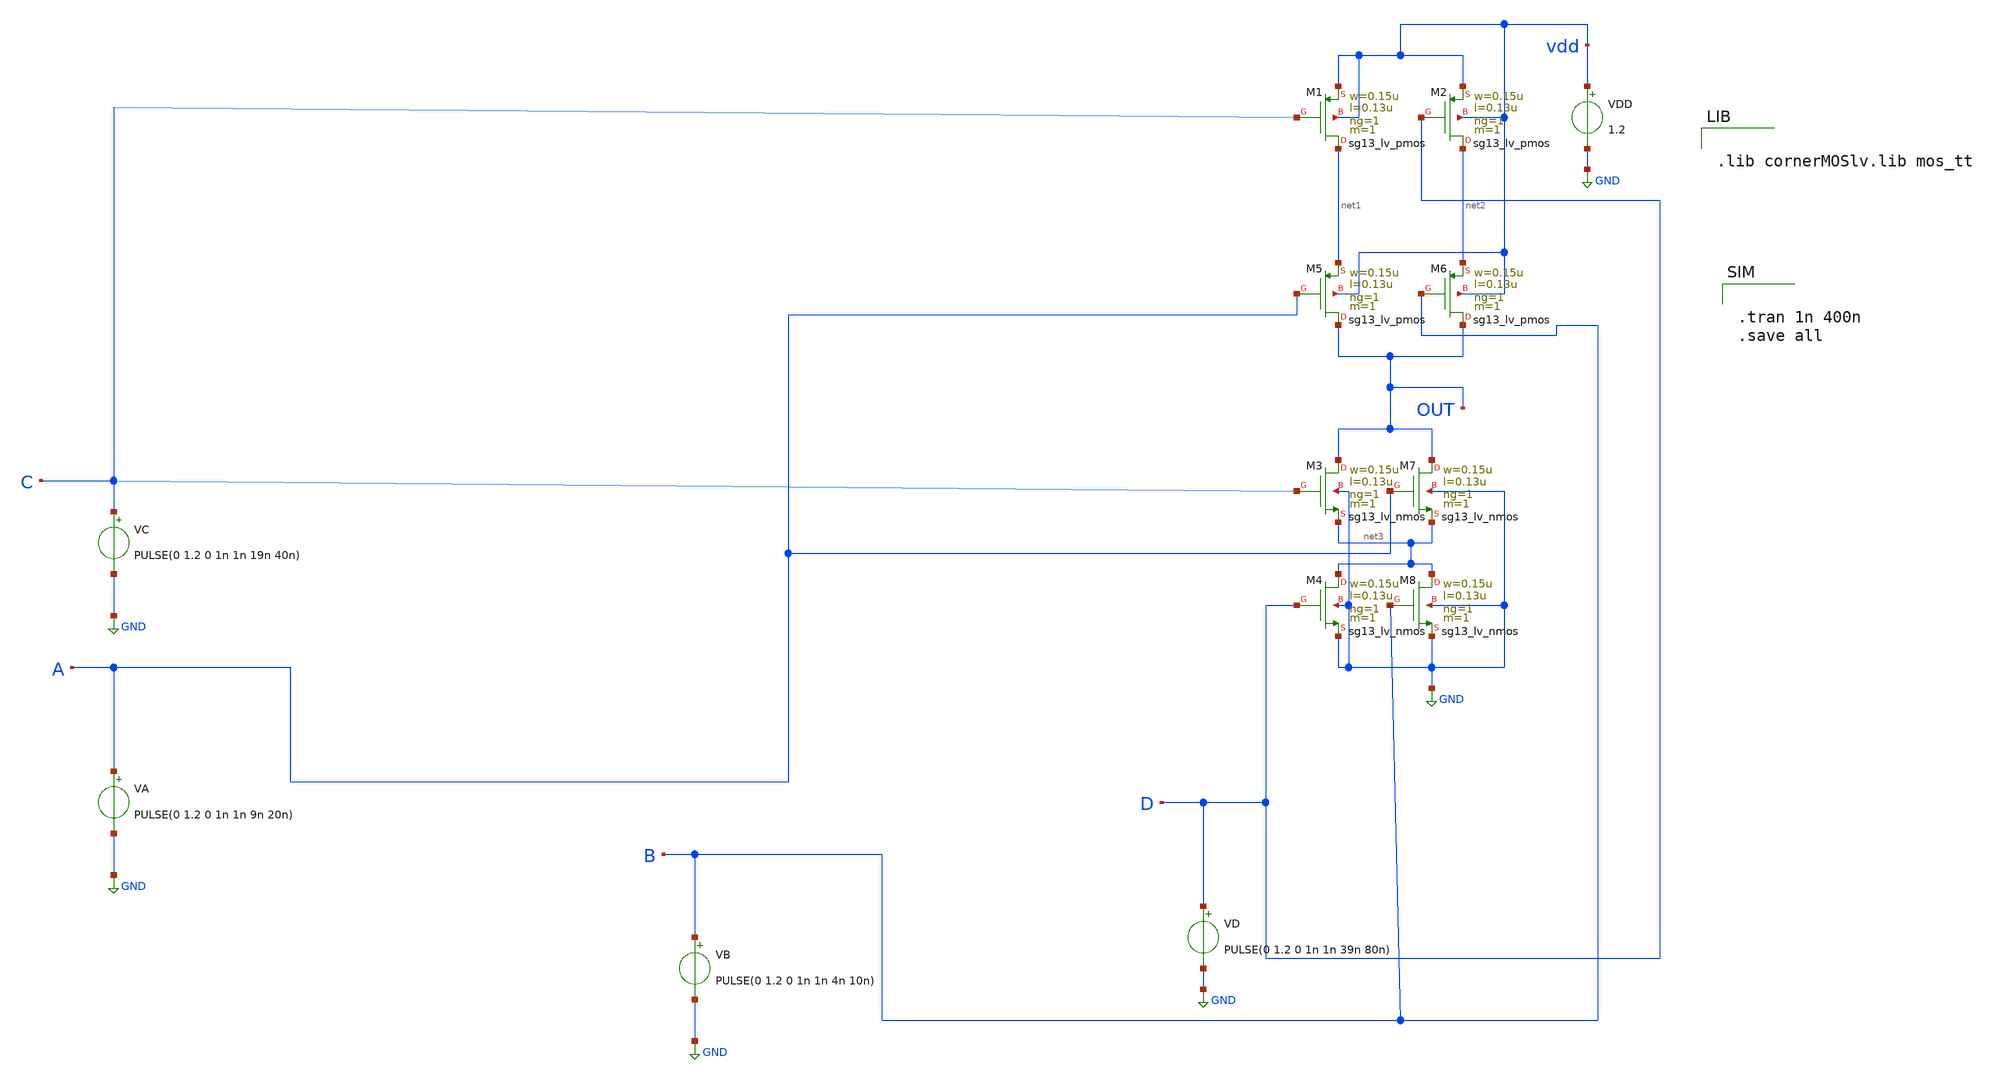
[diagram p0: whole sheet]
** sch_path: oai22.sch
**.subckt oai22
XM1 net1 C vdd vdd sg13_lv_pmos w=0.15u l=0.13u ng=1 m=1 mm_ok=1
XM2 net2 D vdd vdd sg13_lv_pmos w=0.15u l=0.13u ng=1 m=1 mm_ok=1
XM3 OUT C net3 GND sg13_lv_nmos w=0.15u l=0.13u ng=1 m=1 mm_ok=1
XM4 net3 D GND GND sg13_lv_nmos w=0.15u l=0.13u ng=1 m=1 mm_ok=1
VDD vdd GND 1.2
VA A GND PULSE(0 1.2 0 1n 1n 9n 20n)
VB B GND PULSE(0 1.2 0 1n 1n 4n 10n)
XM5 OUT A net1 vdd sg13_lv_pmos w=0.15u l=0.13u ng=1 m=1 mm_ok=1
XM6 OUT B net2 vdd sg13_lv_pmos w=0.15u l=0.13u ng=1 m=1 mm_ok=1
XM7 OUT A net3 GND sg13_lv_nmos w=0.15u l=0.13u ng=1 m=1 mm_ok=1
XM8 net3 B GND GND sg13_lv_nmos w=0.15u l=0.13u ng=1 m=1 mm_ok=1
VC C GND PULSE(0 1.2 0 1n 1n 19n 40n)
VD D GND PULSE(0 1.2 0 1n 1n 39n 80n)
**** begin user architecture code


.lib cornerMOSlv.lib mos_tt



.tran 1n 400n
.save all


**** end user architecture code
**.ends
.GLOBAL GND
.end
